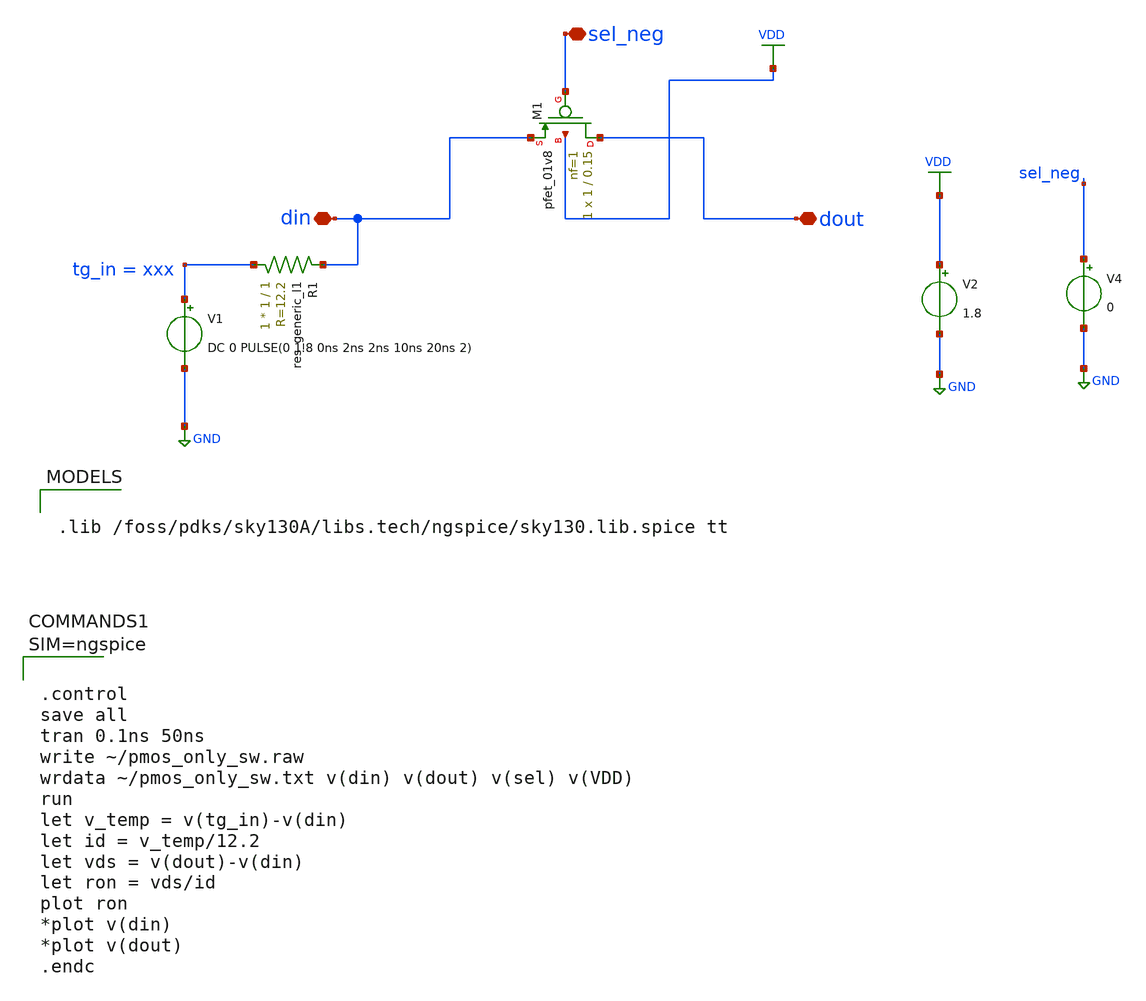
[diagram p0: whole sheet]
** sch_path: tseng_workspace/transmission_gate/schematic/spice/pmos_only_sw.sch
**.subckt pmos_only_sw din dout sel_neg
*.iopin din
*.iopin dout
*.iopin sel_neg
XM1 dout sel_neg din VDD sky130_fd_pr__pfet_01v8 L=0.15 W=1 nf=1 ad='int((nf+1)/2) * W/nf * 0.29' as='int((nf+2)/2) * W/nf * 0.29'
+ pd='2*int((nf+1)/2) * (W/nf + 0.29)' ps='2*int((nf+2)/2) * (W/nf + 0.29)' nrd='0.29 / W' nrs='0.29 / W'
+ sa=0 sb=0 sd=0 mult=1 m=1
V2 VDD GND 1.8
V4 sel_neg GND 0
V1 tg_in GND DC 0 PULSE(0 1.8 0ns 2ns 2ns 10ns 20ns 2)
R1 tg_in din sky130_fd_pr__res_generic_l1 W=1 L=1 m=1
**** begin user architecture code

.lib /foss/pdks/sky130A/libs.tech/ngspice/sky130.lib.spice tt




.control
save all
tran 0.1ns 50ns
write ~/pmos_only_sw.raw
wrdata ~/pmos_only_sw.txt v(din) v(dout) v(sel) v(VDD)
run
let v_temp = v(tg_in)-v(din)
let id = v_temp/12.2
let vds = v(dout)-v(din)
let ron = vds/id
plot ron
*plot v(din)
*plot v(dout)
.endc



**** end user architecture code
**.ends
.GLOBAL VDD
.GLOBAL GND
.end
